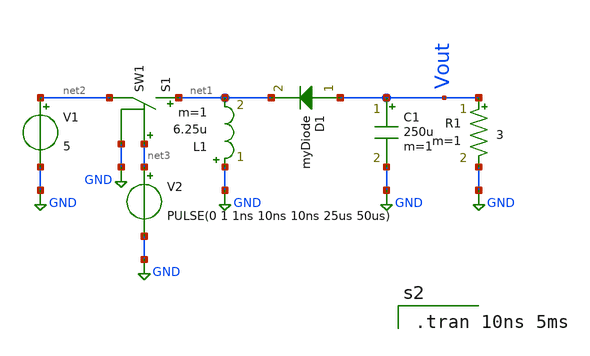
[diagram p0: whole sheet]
** sch_path: Xschem/buck_boost_conv.sch
**.subckt buck_boost_conv
S1 net1 net2 net3 GND SW1
C1 Vout GND 250u m=1
R1 Vout GND 3 m=1
L1 GND net1 6.25u m=1
D1 Vout net1 myDiode area=1
V1 net2 GND 5
V2 net3 GND PULSE(0 1 1ns 10ns 10ns 25us 50us)
**** begin user architecture code

.tran 10ns 5ms


.model myDiode D (IS=2.52n N=1.752 RS=0.568 CJO=4p BV=100 IBV=0.1p TT=4n)

**** end user architecture code
**.ends
.GLOBAL GND
**** begin user architecture code
.MODEL SW1 SW( VT=0.9 VH=0.01 RON=0.01 ROFF=10G )
**** end user architecture code
.end
